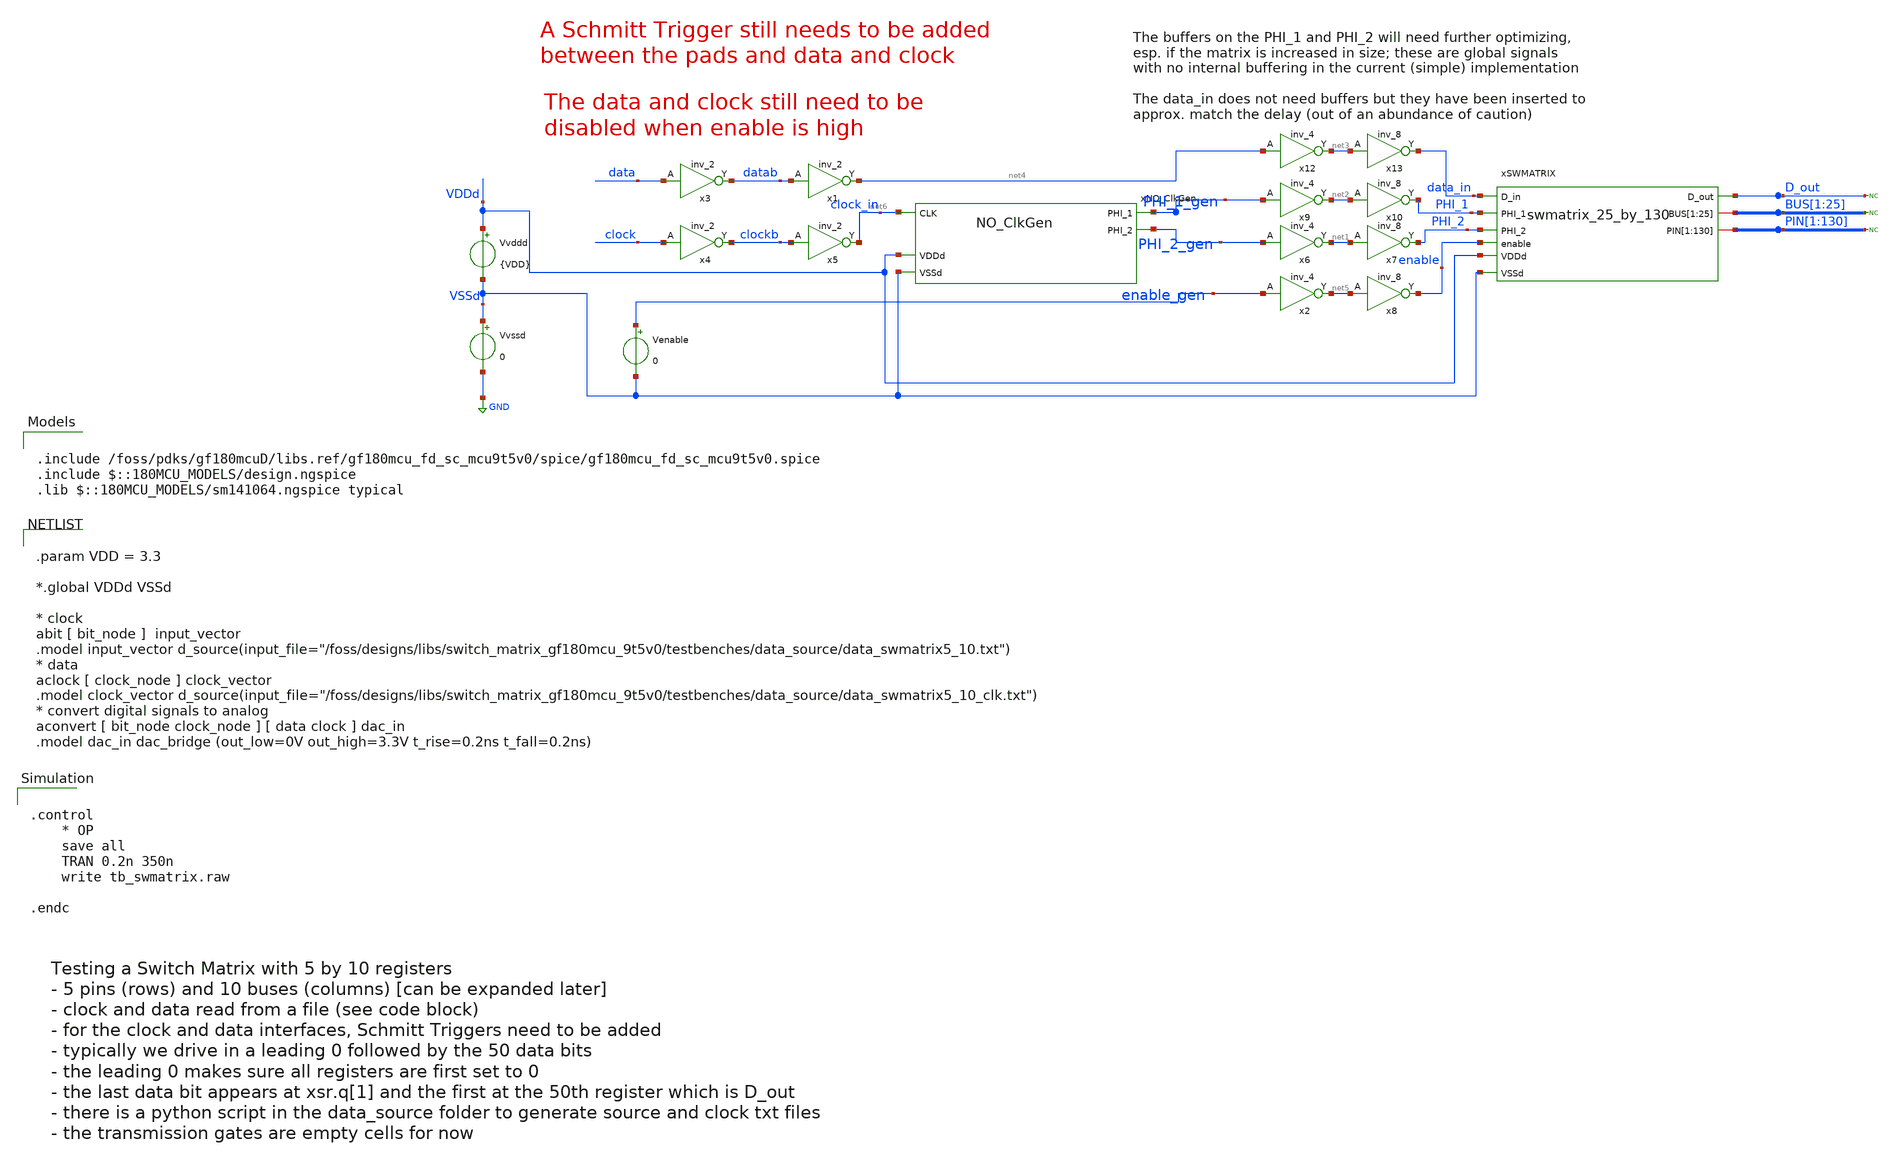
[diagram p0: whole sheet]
** sch_path: testbenches/tb_swmatrix_MOSbiusV3.sch
**.subckt tb_swmatrix_MOSbiusV3
Vvssd VSSd GND 0
Vvddd VDDd VSSd {VDD}
xNO_ClkGen PHI_2_gen net6 PHI_1_gen VDDd VSSd NO_ClkGen
x3 data VSSd VDDd VSSd VDDd datab gf180mcu_fd_sc_mcu9t5v0__inv_2
x1 datab VSSd VDDd VSSd VDDd net4 gf180mcu_fd_sc_mcu9t5v0__inv_2
x4 clock VSSd VDDd VSSd VDDd clockb gf180mcu_fd_sc_mcu9t5v0__inv_2
x5 clockb VSSd VDDd VSSd VDDd net6 gf180mcu_fd_sc_mcu9t5v0__inv_2
xSWMATRIX data_in D_out PHI_1 PHI_2 BUS[1] BUS[2] BUS[3] BUS[4] BUS[5] BUS[6] BUS[7] BUS[8] BUS[9]
+ BUS[10] BUS[11] BUS[12] BUS[13] BUS[14] BUS[15] BUS[16] BUS[17] BUS[18] BUS[19] BUS[20] BUS[21] BUS[22]
+ BUS[23] BUS[24] BUS[25] PIN[1] PIN[2] PIN[3] PIN[4] PIN[5] PIN[6] PIN[7] PIN[8] PIN[9] PIN[10] PIN[11]
+ PIN[12] PIN[13] PIN[14] PIN[15] PIN[16] PIN[17] PIN[18] PIN[19] PIN[20] PIN[21] PIN[22] PIN[23] PIN[24]
+ PIN[25] PIN[26] PIN[27] PIN[28] PIN[29] PIN[30] PIN[31] PIN[32] PIN[33] PIN[34] PIN[35] PIN[36] PIN[37]
+ PIN[38] PIN[39] PIN[40] PIN[41] PIN[42] PIN[43] PIN[44] PIN[45] PIN[46] PIN[47] PIN[48] PIN[49] PIN[50]
+ PIN[51] PIN[52] PIN[53] PIN[54] PIN[55] PIN[56] PIN[57] PIN[58] PIN[59] PIN[60] PIN[61] PIN[62] PIN[63]
+ PIN[64] PIN[65] PIN[66] PIN[67] PIN[68] PIN[69] PIN[70] PIN[71] PIN[72] PIN[73] PIN[74] PIN[75] PIN[76]
+ PIN[77] PIN[78] PIN[79] PIN[80] PIN[81] PIN[82] PIN[83] PIN[84] PIN[85] PIN[86] PIN[87] PIN[88] PIN[89]
+ PIN[90] PIN[91] PIN[92] PIN[93] PIN[94] PIN[95] PIN[96] PIN[97] PIN[98] PIN[99] PIN[100] PIN[101] PIN[102]
+ PIN[103] PIN[104] PIN[105] PIN[106] PIN[107] PIN[108] PIN[109] PIN[110] PIN[111] PIN[112] PIN[113] PIN[114]
+ PIN[115] PIN[116] PIN[117] PIN[118] PIN[119] PIN[120] PIN[121] PIN[122] PIN[123] PIN[124] PIN[125] PIN[126]
+ PIN[127] PIN[128] PIN[129] PIN[130] VDDd VSSd enable swmatrix_25_by_130
* noconn D_out
* noconn BUS[1:25]
* noconn PIN[1:130]
x6 PHI_2_gen VSSd VDDd VSSd VDDd net1 gf180mcu_fd_sc_mcu9t5v0__inv_4
x7 net1 VSSd VDDd VSSd VDDd PHI_2 gf180mcu_fd_sc_mcu9t5v0__inv_8
x9 PHI_1_gen VSSd VDDd VSSd VDDd net2 gf180mcu_fd_sc_mcu9t5v0__inv_4
x10 net2 VSSd VDDd VSSd VDDd PHI_1 gf180mcu_fd_sc_mcu9t5v0__inv_8
x12 net4 VSSd VDDd VSSd VDDd net3 gf180mcu_fd_sc_mcu9t5v0__inv_4
x13 net3 VSSd VDDd VSSd VDDd data_in gf180mcu_fd_sc_mcu9t5v0__inv_8
x2 enable_gen VSSd VDDd VSSd VDDd net5 gf180mcu_fd_sc_mcu9t5v0__inv_4
x8 net5 VSSd VDDd VSSd VDDd enable gf180mcu_fd_sc_mcu9t5v0__inv_8
Venable enable_gen VSSd 0
**** begin user architecture code


.control
    * OP
    save all
    TRAN 0.2n 350n
    write tb_swmatrix.raw

.endc



.include /foss/pdks/gf180mcuD/libs.ref/gf180mcu_fd_sc_mcu9t5v0/spice/gf180mcu_fd_sc_mcu9t5v0.spice
.include $::180MCU_MODELS/design.ngspice
.lib $::180MCU_MODELS/sm141064.ngspice typical



.param VDD = 3.3

*.global VDDd VSSd

* clock
abit [ bit_node ]  input_vector
.model input_vector
+ d_source(input_file="/foss/designs/libs/switch_matrix_gf180mcu_9t5v0/testbenches/data_source/data_swmatrix5_10.txt")
* data
aclock [ clock_node ] clock_vector
.model clock_vector
+ d_source(input_file="/foss/designs/libs/switch_matrix_gf180mcu_9t5v0/testbenches/data_source/data_swmatrix5_10_clk.txt")
* convert digital signals to analog
aconvert [ bit_node clock_node ] [ data clock ] dac_in
.model dac_in dac_bridge (out_low=0V out_high=3.3V t_rise=0.2ns t_fall=0.2ns)


**** end user architecture code
**.ends
.GLOBAL GND
.end
